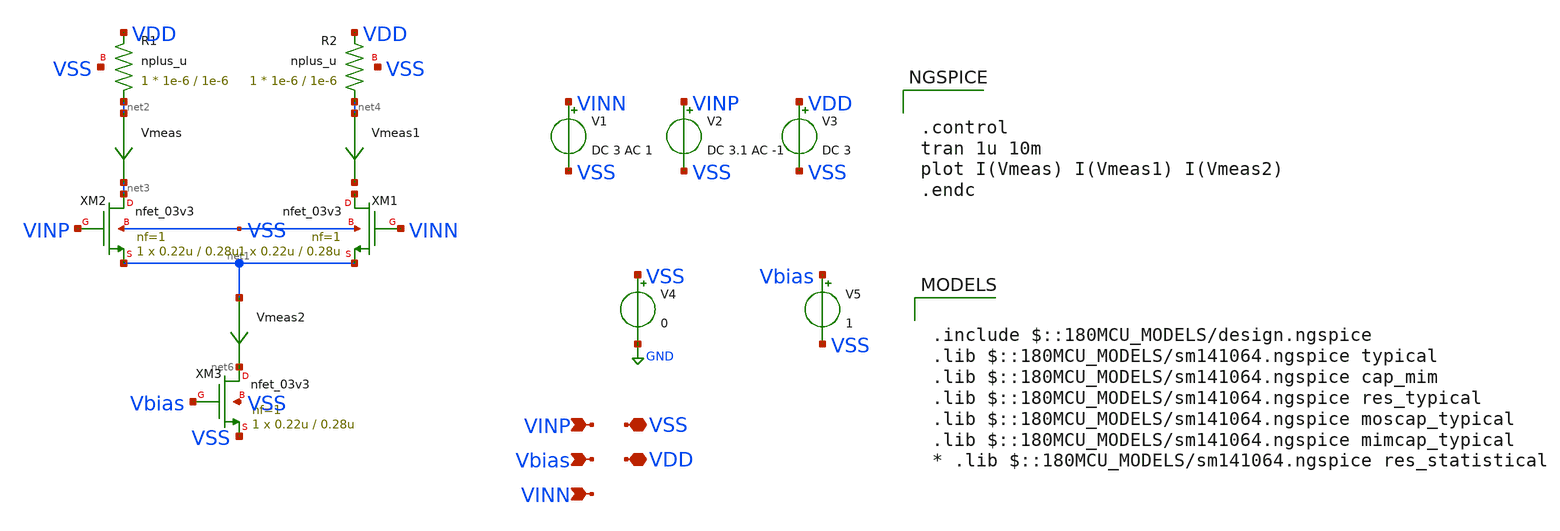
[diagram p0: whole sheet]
** sch_path: week03_small_signal_amp/tugas9_ac_sweep_response/diff-pair.sch
**.subckt diff-pair VSS VDD VINP Vbias VINN
*.iopin VSS
*.iopin VDD
*.ipin VINP
*.ipin Vbias
*.ipin VINN
XM1 net5 VINN net1 VSS nfet_03v3 L=0.28u W=0.22u nf=1 ad='int((nf+1)/2) * W/nf * 0.18u' as='int((nf+2)/2) * W/nf * 0.18u'
+ pd='2*int((nf+1)/2) * (W/nf + 0.18u)' ps='2*int((nf+2)/2) * (W/nf + 0.18u)' nrd='0.18u / W' nrs='0.18u / W'
+ sa=0 sb=0 sd=0 m=1
XM2 net3 VINP net1 VSS nfet_03v3 L=0.28u W=0.22u nf=1 ad='int((nf+1)/2) * W/nf * 0.18u' as='int((nf+2)/2) * W/nf * 0.18u'
+ pd='2*int((nf+1)/2) * (W/nf + 0.18u)' ps='2*int((nf+2)/2) * (W/nf + 0.18u)' nrd='0.18u / W' nrs='0.18u / W'
+ sa=0 sb=0 sd=0 m=1
XM3 net6 Vbias VSS VSS nfet_03v3 L=0.28u W=0.22u nf=1 ad='int((nf+1)/2) * W/nf * 0.18u' as='int((nf+2)/2) * W/nf * 0.18u'
+ pd='2*int((nf+1)/2) * (W/nf + 0.18u)' ps='2*int((nf+2)/2) * (W/nf + 0.18u)' nrd='0.18u / W' nrs='0.18u / W'
+ sa=0 sb=0 sd=0 m=1
XR1 net2 VDD VSS nplus_u r_width=1e-6 r_length=1e-6 m=1
XR2 net4 VDD VSS nplus_u r_width=1e-6 r_length=1e-6 m=1
V1 VINN VSS DC 3 AC 1
V2 VINP VSS DC 3.1 AC -1
V3 VDD VSS DC 3
V4 VSS GND 0
V5 Vbias VSS 1
Vmeas net2 net3 0
.save i(vmeas)
Vmeas1 net4 net7 0
.save i(vmeas1)
Vmeas2 net1 net6 0
.save i(vmeas2)
**** begin user architecture code

.include $::180MCU_MODELS/design.ngspice
.lib $::180MCU_MODELS/sm141064.ngspice typical
.lib $::180MCU_MODELS/sm141064.ngspice cap_mim
.lib $::180MCU_MODELS/sm141064.ngspice res_typical
.lib $::180MCU_MODELS/sm141064.ngspice moscap_typical
.lib $::180MCU_MODELS/sm141064.ngspice mimcap_typical
* .lib $::180MCU_MODELS/sm141064.ngspice res_statistical



.control
tran 1u 10m
plot I(Vmeas) I(Vmeas1) I(Vmeas2)
.endc


**** end user architecture code
**.ends
.GLOBAL GND
.end
